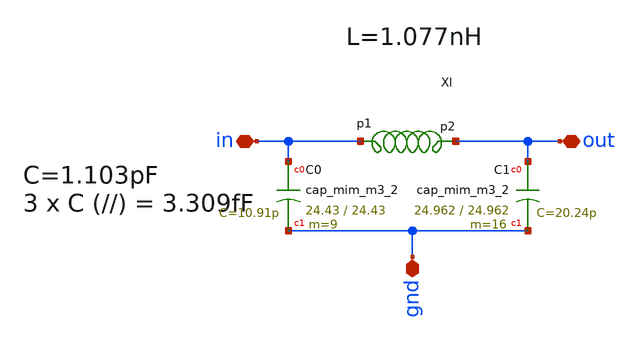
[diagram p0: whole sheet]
** sch_path: impedance-transformer/xschem/impedance-transformer.sch
**.subckt impedance-transformer gnd in out
*.iopin gnd
*.iopin in
*.iopin out
XC0 in gnd sky130_fd_pr__cap_mim_m3_2 W=24.43 L=24.43 MF=9 m=9
XC1 out gnd sky130_fd_pr__cap_mim_m3_2 W=24.962 L=24.962 MF=16 m=16
x1 in out l1
**.ends

* expanding   symbol:  /home/hugodg/projects_sky130/temp_sensor/impedance-transformer/xschem/l1.sym
*+ # of pins=2
** sym_path: impedance-transformer/xschem/l1.sym
** sch_path: impedance-transformer/xschem/l1.sch
.subckt l1 p1 p2
*.iopin p2
*.iopin p1
L0 p1 net3 592.7p m=1
Cs1 p1 net1 26.83f m=1
Cs2 p2 net2 24.25f m=1
Rs1 net1 GND 65.02 m=1
Rs2 net2 GND 14.4 m=1
R1 p2 net3 2.935 m=1
.ends

.GLOBAL GND
.end
